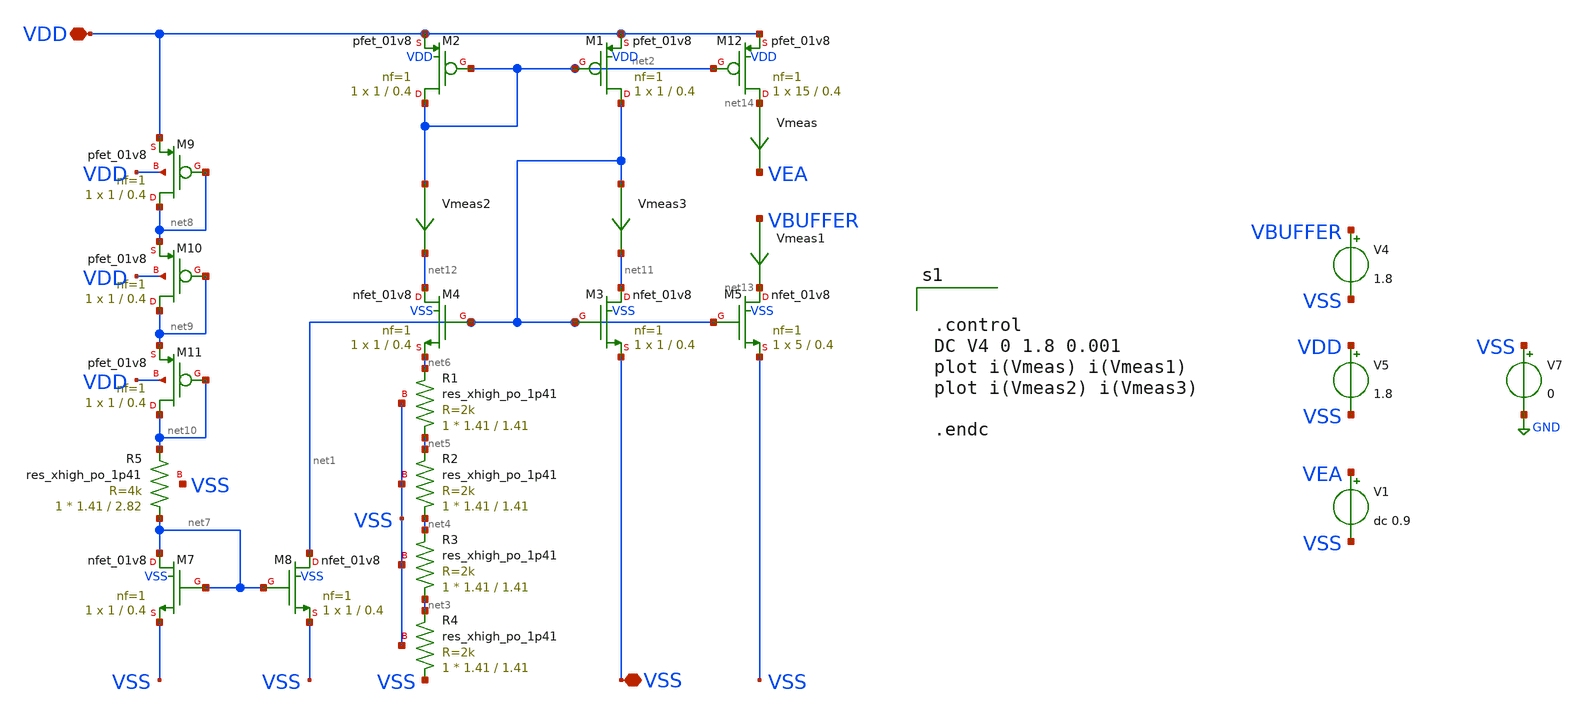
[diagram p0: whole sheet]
** sch_path: xschem/bias-net/schematics/bias-network.sch
**.subckt bias-network VSS VDD
*.iopin VSS
*.iopin VDD
XR1 net5 net6 VSS sky130_fd_pr__res_xhigh_po_1p41 L=1.41 mult=1 m=1
XR2 net4 net5 VSS sky130_fd_pr__res_xhigh_po_1p41 L=1.41 mult=1 m=1
XR3 net3 net4 VSS sky130_fd_pr__res_xhigh_po_1p41 L=1.41 mult=1 m=1
XR4 VSS net3 VSS sky130_fd_pr__res_xhigh_po_1p41 L=1.41 mult=1 m=1
XM3 net11 net1 VSS VSS sky130_fd_pr__nfet_01v8 L=0.4 W=1 nf=1 ad='int((nf+1)/2) * W/nf * 0.29' as='int((nf+2)/2) * W/nf * 0.29'
+ pd='2*int((nf+1)/2) * (W/nf + 0.29)' ps='2*int((nf+2)/2) * (W/nf + 0.29)' nrd='0.29 / W' nrs='0.29 / W'
+ sa=0 sb=0 sd=0 mult=1 m=1
XM4 net12 net1 net6 VSS sky130_fd_pr__nfet_01v8 L=0.4 W=1 nf=1 ad='int((nf+1)/2) * W/nf * 0.29' as='int((nf+2)/2) * W/nf * 0.29'
+ pd='2*int((nf+1)/2) * (W/nf + 0.29)' ps='2*int((nf+2)/2) * (W/nf + 0.29)' nrd='0.29 / W' nrs='0.29 / W'
+ sa=0 sb=0 sd=0 mult=1 m=1
XM5 net13 net1 VSS VSS sky130_fd_pr__nfet_01v8 L=0.4 W=5 nf=1 ad='int((nf+1)/2) * W/nf * 0.29' as='int((nf+2)/2) * W/nf * 0.29'
+ pd='2*int((nf+1)/2) * (W/nf + 0.29)' ps='2*int((nf+2)/2) * (W/nf + 0.29)' nrd='0.29 / W' nrs='0.29 / W'
+ sa=0 sb=0 sd=0 mult=1 m=1
Vmeas net14 VEA 0
.save i(vmeas)
Vmeas1 VBUFFER net13 0
.save i(vmeas1)
XM7 net7 net7 VSS VSS sky130_fd_pr__nfet_01v8 L=0.4 W=1 nf=1 ad='int((nf+1)/2) * W/nf * 0.29' as='int((nf+2)/2) * W/nf * 0.29'
+ pd='2*int((nf+1)/2) * (W/nf + 0.29)' ps='2*int((nf+2)/2) * (W/nf + 0.29)' nrd='0.29 / W' nrs='0.29 / W'
+ sa=0 sb=0 sd=0 mult=1 m=1
XM8 net1 net7 VSS VSS sky130_fd_pr__nfet_01v8 L=0.4 W=1 nf=1 ad='int((nf+1)/2) * W/nf * 0.29' as='int((nf+2)/2) * W/nf * 0.29'
+ pd='2*int((nf+1)/2) * (W/nf + 0.29)' ps='2*int((nf+2)/2) * (W/nf + 0.29)' nrd='0.29 / W' nrs='0.29 / W'
+ sa=0 sb=0 sd=0 mult=1 m=1
XR5 net7 net10 VSS sky130_fd_pr__res_xhigh_po_1p41 L=2.82 mult=1 m=1
V5 VDD VSS 1.8
V7 VSS GND 0
V1 VEA VSS dc 0.9
V4 VBUFFER VSS 1.8
XM9 net8 net8 VDD VDD sky130_fd_pr__pfet_01v8 L=0.4 W=1 nf=1 ad='int((nf+1)/2) * W/nf * 0.29' as='int((nf+2)/2) * W/nf * 0.29'
+ pd='2*int((nf+1)/2) * (W/nf + 0.29)' ps='2*int((nf+2)/2) * (W/nf + 0.29)' nrd='0.29 / W' nrs='0.29 / W'
+ sa=0 sb=0 sd=0 mult=1 m=1
XM10 net9 net9 net8 VDD sky130_fd_pr__pfet_01v8 L=0.4 W=1 nf=1 ad='int((nf+1)/2) * W/nf * 0.29' as='int((nf+2)/2) * W/nf * 0.29'
+ pd='2*int((nf+1)/2) * (W/nf + 0.29)' ps='2*int((nf+2)/2) * (W/nf + 0.29)' nrd='0.29 / W' nrs='0.29 / W'
+ sa=0 sb=0 sd=0 mult=1 m=1
XM11 net10 net10 net9 VDD sky130_fd_pr__pfet_01v8 L=0.4 W=1 nf=1 ad='int((nf+1)/2) * W/nf * 0.29' as='int((nf+2)/2) * W/nf * 0.29'
+ pd='2*int((nf+1)/2) * (W/nf + 0.29)' ps='2*int((nf+2)/2) * (W/nf + 0.29)' nrd='0.29 / W' nrs='0.29 / W'
+ sa=0 sb=0 sd=0 mult=1 m=1
Vmeas2 net2 net12 0
.save i(vmeas2)
Vmeas3 net1 net11 0
.save i(vmeas3)
XM1 net1 net2 VDD VDD sky130_fd_pr__pfet_01v8 L=0.4 W=1 nf=1 ad='int((nf+1)/2) * W/nf * 0.29' as='int((nf+2)/2) * W/nf * 0.29'
+ pd='2*int((nf+1)/2) * (W/nf + 0.29)' ps='2*int((nf+2)/2) * (W/nf + 0.29)' nrd='0.29 / W' nrs='0.29 / W'
+ sa=0 sb=0 sd=0 mult=1 m=1
XM2 net2 net2 VDD VDD sky130_fd_pr__pfet_01v8 L=0.4 W=1 nf=1 ad='int((nf+1)/2) * W/nf * 0.29' as='int((nf+2)/2) * W/nf * 0.29'
+ pd='2*int((nf+1)/2) * (W/nf + 0.29)' ps='2*int((nf+2)/2) * (W/nf + 0.29)' nrd='0.29 / W' nrs='0.29 / W'
+ sa=0 sb=0 sd=0 mult=1 m=1
XM12 net14 net2 VDD VDD sky130_fd_pr__pfet_01v8 L=0.4 W=15 nf=1 ad='int((nf+1)/2) * W/nf * 0.29' as='int((nf+2)/2) * W/nf * 0.29'
+ pd='2*int((nf+1)/2) * (W/nf + 0.29)' ps='2*int((nf+2)/2) * (W/nf + 0.29)' nrd='0.29 / W' nrs='0.29 / W'
+ sa=0 sb=0 sd=0 mult=1 m=1
**** begin user architecture code


.control
DC V4 0 1.8 0.001
plot i(Vmeas) i(Vmeas1)
plot i(Vmeas2) i(Vmeas3)

.endc



** opencircuitdesign pdks install
.lib $::SKYWATER_MODELS/sky130.lib.spice tt


**** end user architecture code
**.ends
.GLOBAL GND
.end
